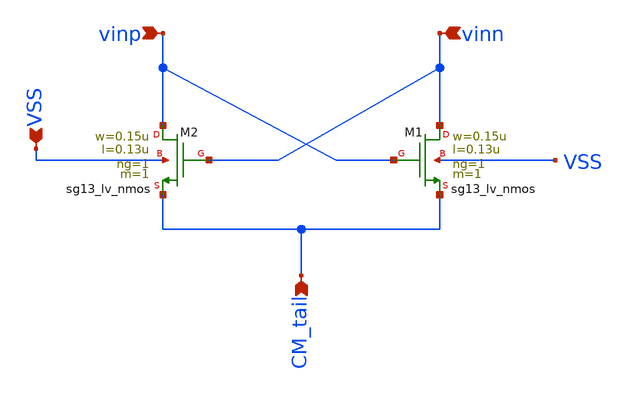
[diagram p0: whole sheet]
** sch_path: analog-db/templates/miscellaneous/cross_coupled_nmos.sch
**.subckt cross_coupled_nmos vinp vinn CM_tail VSS
*.ipin vinp
*.ipin vinn
*.ipin CM_tail
*.ipin VSS
XM1 vinn vinp CM_tail VSS sg13_lv_nmos w=0.15u l=0.13u ng=1 m=1 mm_ok=1
XM2 vinp vinn CM_tail VSS sg13_lv_nmos w=0.15u l=0.13u ng=1 m=1 mm_ok=1
**.ends
.end
